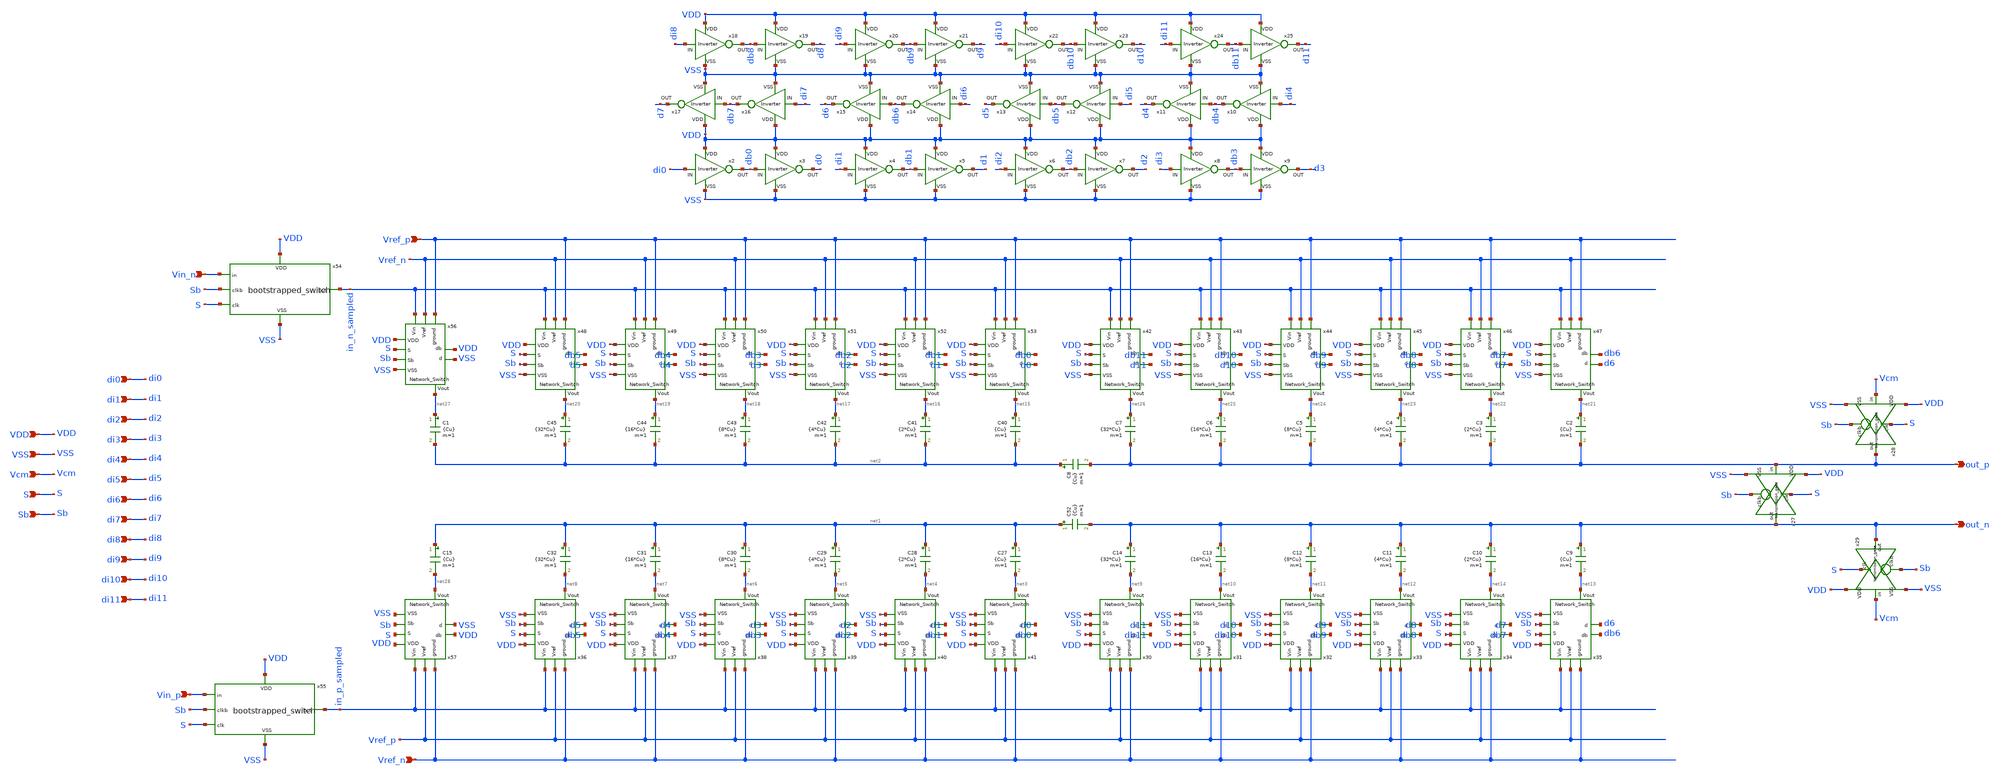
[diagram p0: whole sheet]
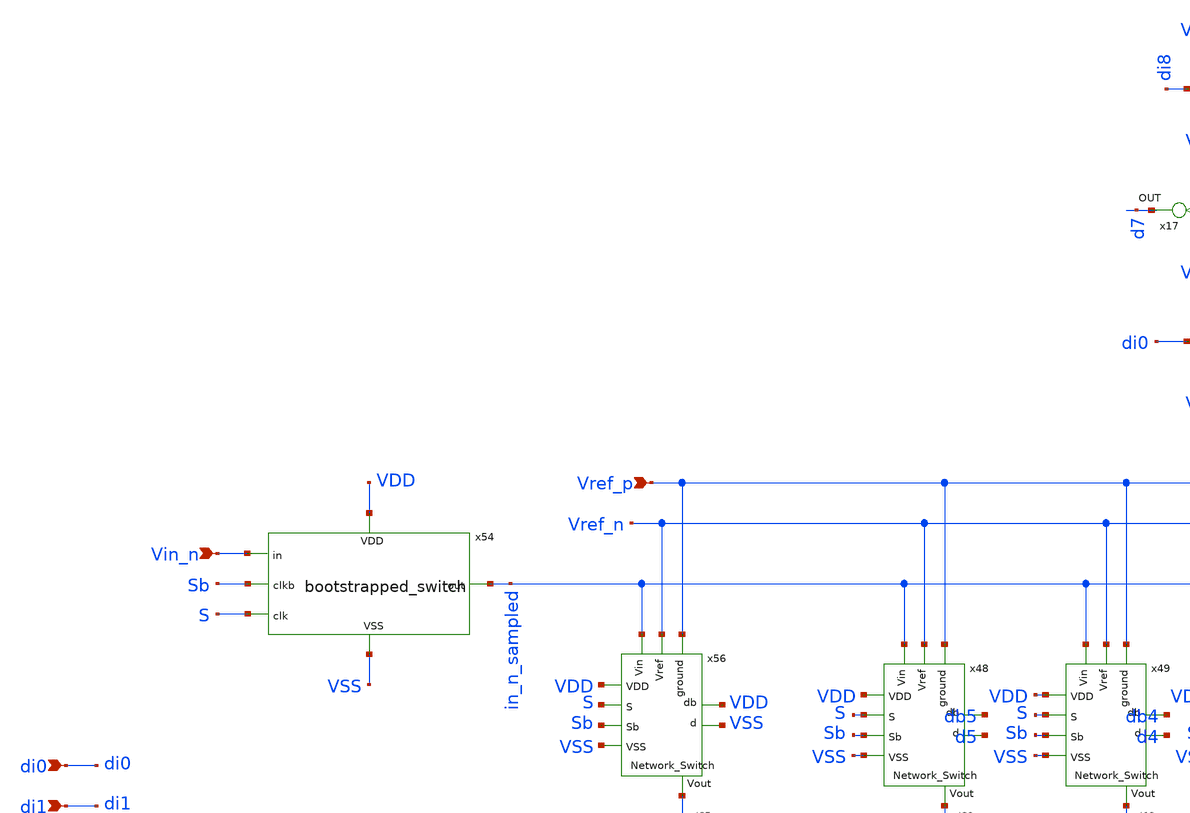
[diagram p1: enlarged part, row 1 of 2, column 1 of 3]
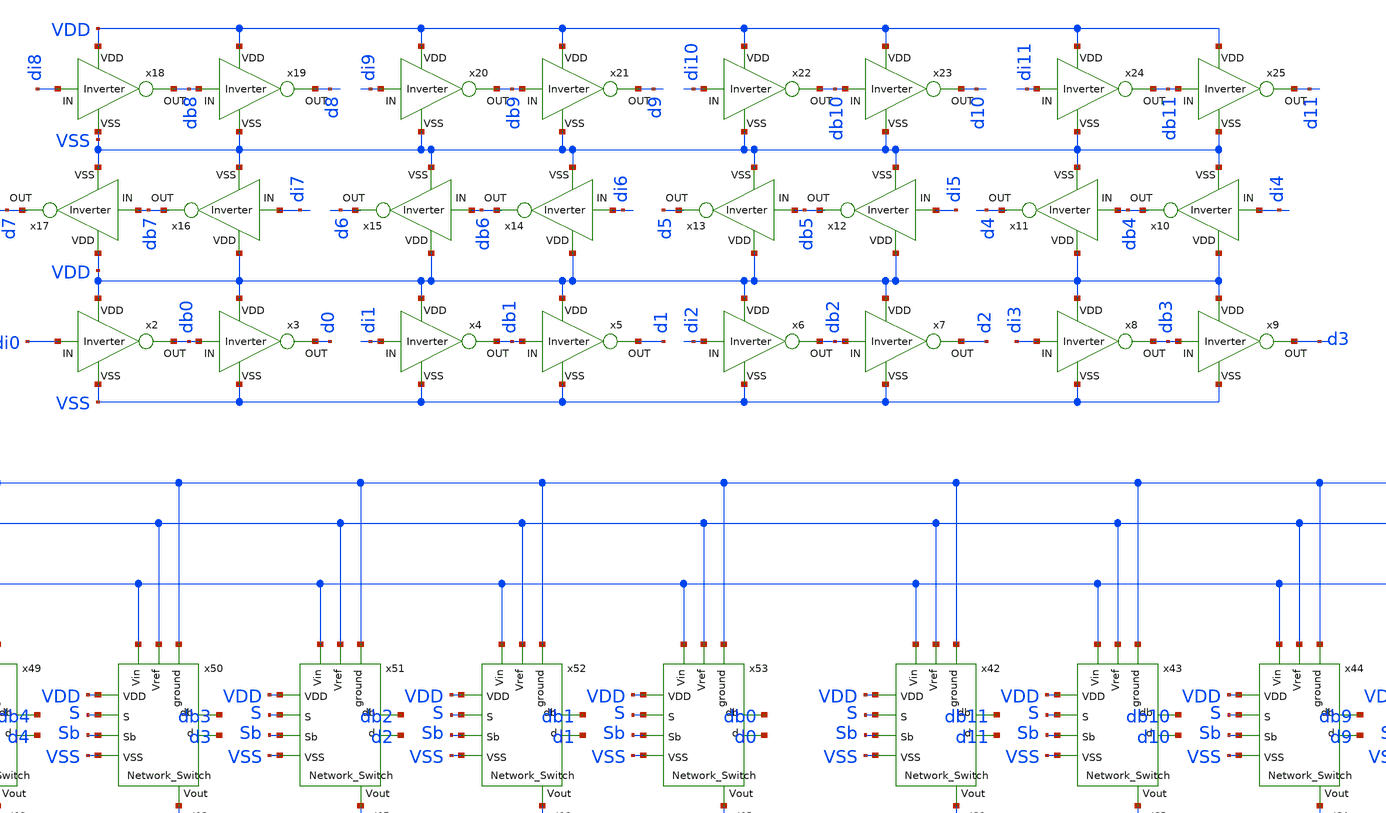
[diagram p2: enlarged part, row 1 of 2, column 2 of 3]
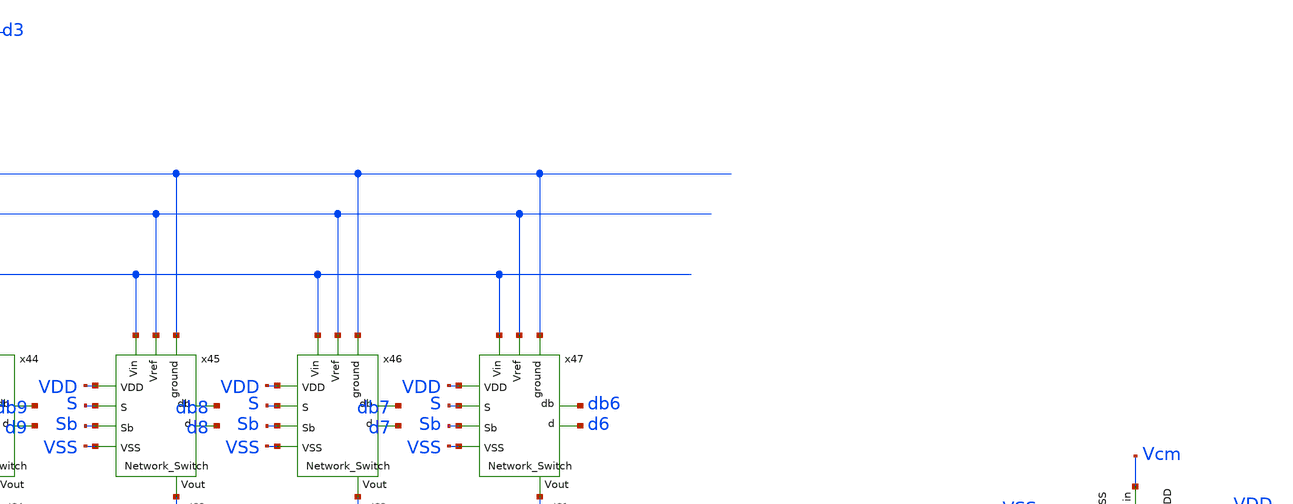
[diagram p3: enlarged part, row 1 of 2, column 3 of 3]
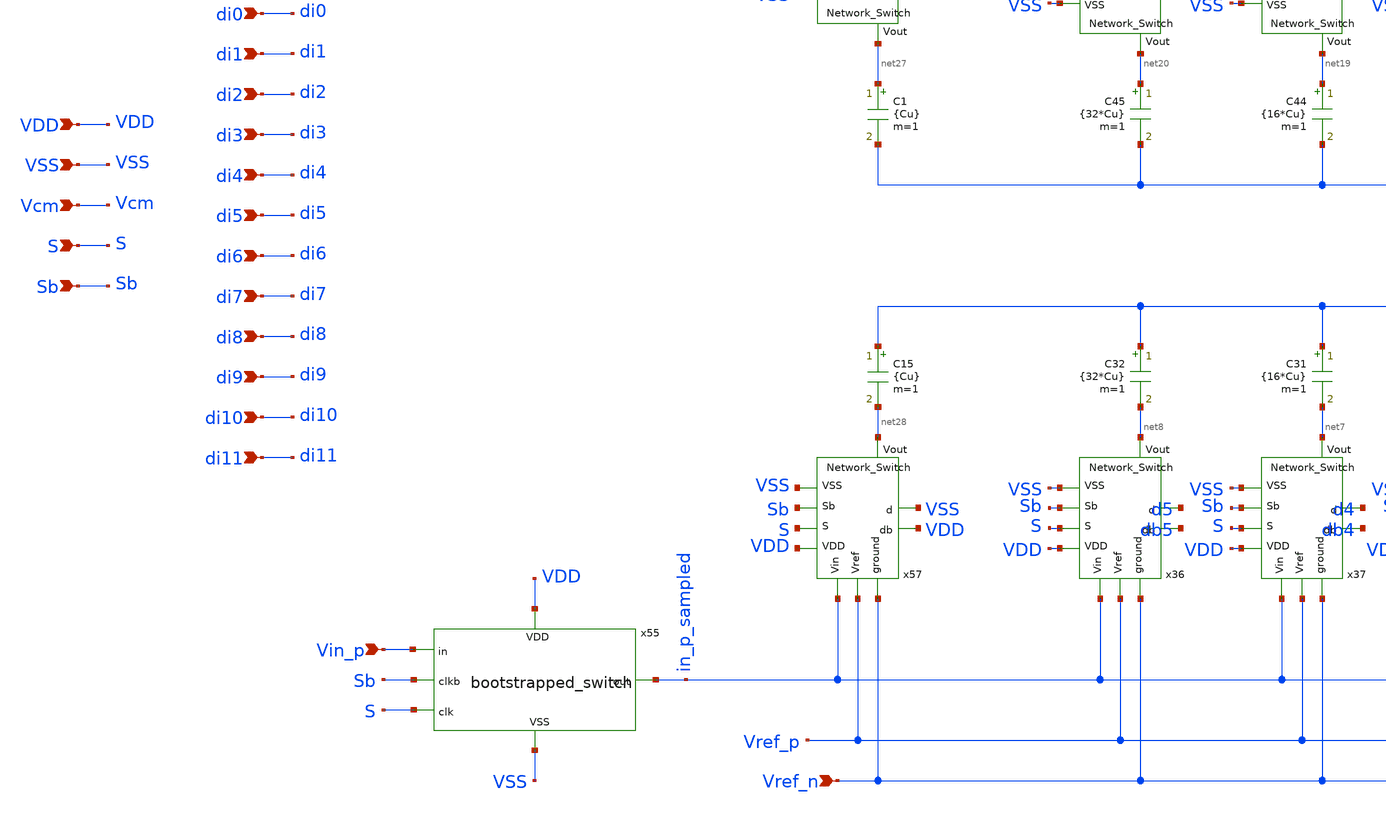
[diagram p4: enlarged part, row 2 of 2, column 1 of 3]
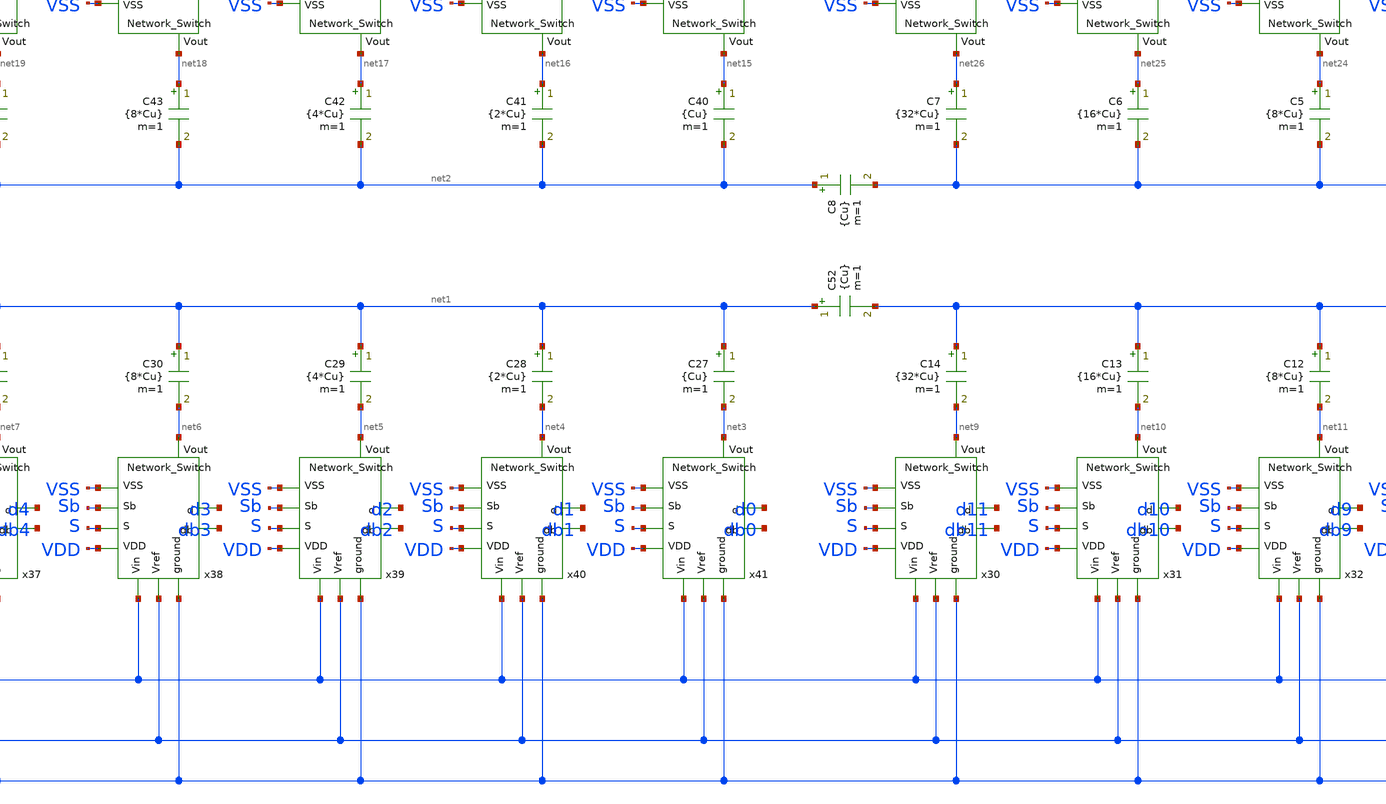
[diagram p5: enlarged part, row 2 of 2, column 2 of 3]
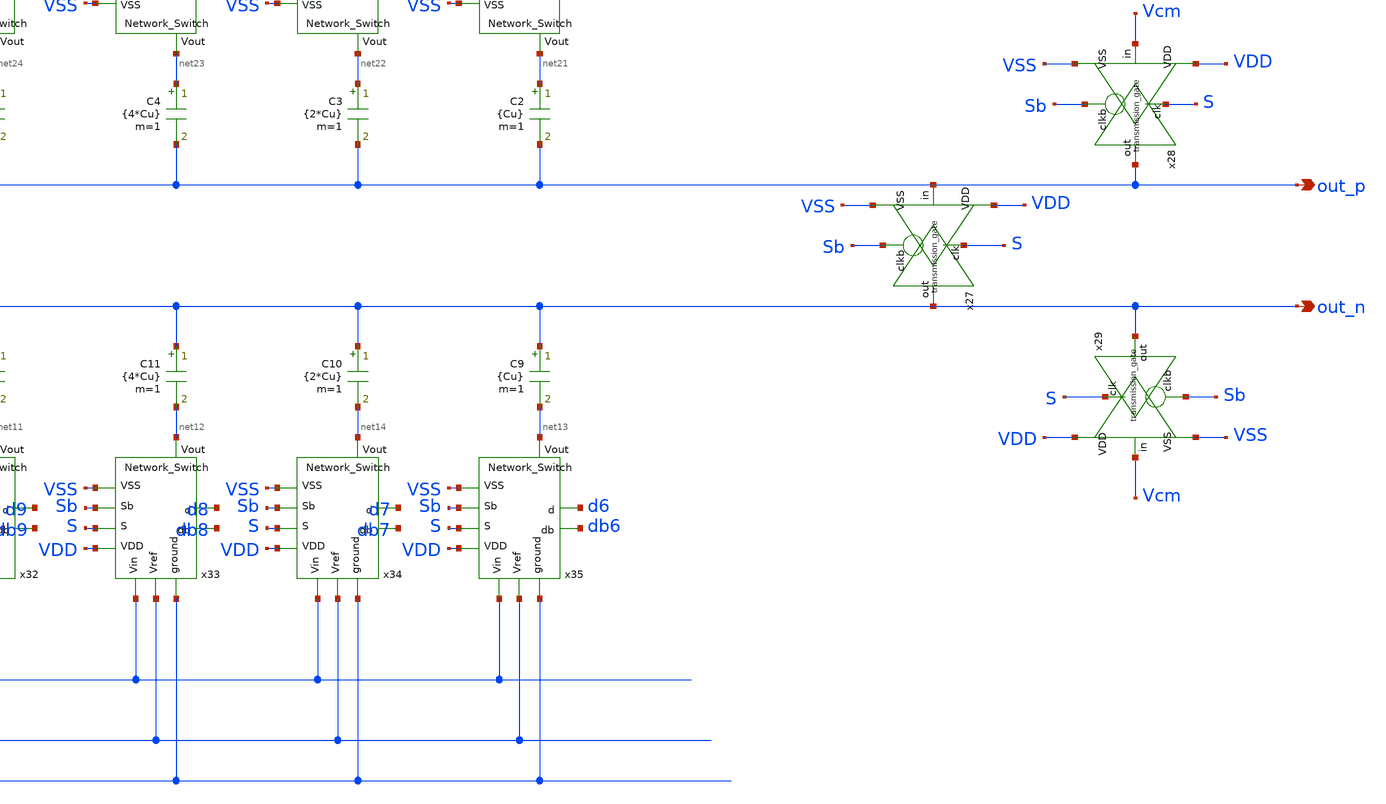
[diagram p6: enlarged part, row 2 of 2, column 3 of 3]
** sch_path: CAP_DAC_ideal_v2.sch
**.subckt CAP_DAC_ideal_v2 VDD VSS S Sb di3 Vcm out_p out_n Vref_p Vref_n di0 di1 di2 di5 di4 di7
*+ di6 di9 di8 di11 di10 Vin_n Vin_p
*.ipin VDD
*.ipin VSS
*.ipin S
*.ipin Sb
*.ipin di3
*.ipin Vcm
*.opin out_p
*.opin out_n
*.ipin Vref_p
*.ipin Vref_n
*.ipin di0
*.ipin di1
*.ipin di2
*.ipin di5
*.ipin di4
*.ipin di7
*.ipin di6
*.ipin di9
*.ipin di8
*.ipin di11
*.ipin di10
*.ipin Vin_n
*.ipin Vin_p
x30 VDD Vref_n Vref_p VSS S Sb d11 db11 in_p_sampled net9 Network_Switch
x31 VDD Vref_n Vref_p VSS S Sb d10 db10 in_p_sampled net10 Network_Switch
x32 VDD Vref_n Vref_p VSS S Sb d9 db9 in_p_sampled net11 Network_Switch
x33 VDD Vref_n Vref_p VSS S Sb d8 db8 in_p_sampled net12 Network_Switch
x34 VDD Vref_n Vref_p VSS S Sb d7 db7 in_p_sampled net14 Network_Switch
x35 VDD Vref_n Vref_p VSS S Sb d6 db6 in_p_sampled net13 Network_Switch
x36 VDD Vref_n Vref_p VSS S Sb d5 db5 in_p_sampled net8 Network_Switch
x37 VDD Vref_n Vref_p VSS S Sb d4 db4 in_p_sampled net7 Network_Switch
x38 VDD Vref_n Vref_p VSS S Sb d3 db3 in_p_sampled net6 Network_Switch
x39 VDD Vref_n Vref_p VSS S Sb d2 db2 in_p_sampled net5 Network_Switch
x40 VDD Vref_n Vref_p VSS S Sb d1 db1 in_p_sampled net4 Network_Switch
x41 VDD Vref_n Vref_p VSS S Sb d0 db0 in_p_sampled net3 Network_Switch
x42 VDD Vref_p Vref_n VSS S Sb d11 db11 in_n_sampled net26 Network_Switch
x43 VDD Vref_p Vref_n VSS S Sb d10 db10 in_n_sampled net25 Network_Switch
x44 VDD Vref_p Vref_n VSS S Sb d9 db9 in_n_sampled net24 Network_Switch
x45 VDD Vref_p Vref_n VSS S Sb d8 db8 in_n_sampled net23 Network_Switch
x46 VDD Vref_p Vref_n VSS S Sb d7 db7 in_n_sampled net22 Network_Switch
x47 VDD Vref_p Vref_n VSS S Sb d6 db6 in_n_sampled net21 Network_Switch
x48 VDD Vref_p Vref_n VSS S Sb d5 db5 in_n_sampled net20 Network_Switch
x49 VDD Vref_p Vref_n VSS S Sb d4 db4 in_n_sampled net19 Network_Switch
x50 VDD Vref_p Vref_n VSS S Sb d3 db3 in_n_sampled net18 Network_Switch
x51 VDD Vref_p Vref_n VSS S Sb d2 db2 in_n_sampled net17 Network_Switch
x52 VDD Vref_p Vref_n VSS S Sb d1 db1 in_n_sampled net16 Network_Switch
x53 VDD Vref_p Vref_n VSS S Sb d0 db0 in_n_sampled net15 Network_Switch
x54 VDD Vin_n Sb S in_n_sampled VSS bootstrapped_switch
x55 VDD Vin_p Sb S in_p_sampled VSS bootstrapped_switch
x27 out_p Sb S VDD VSS out_n transmission_gate
x2 VDD di0 db0 VSS Inverter
x3 VDD db0 d0 VSS Inverter
x4 VDD di1 db1 VSS Inverter
x5 VDD db1 d1 VSS Inverter
x6 VDD di2 db2 VSS Inverter
x7 VDD db2 d2 VSS Inverter
x8 VDD di3 db3 VSS Inverter
x9 VDD db3 d3 VSS Inverter
x10 VDD di4 db4 VSS Inverter
x11 VDD db4 d4 VSS Inverter
x12 VDD di5 db5 VSS Inverter
x13 VDD db5 d5 VSS Inverter
x14 VDD di6 db6 VSS Inverter
x15 VDD db6 d6 VSS Inverter
x16 VDD di7 db7 VSS Inverter
x17 VDD db7 d7 VSS Inverter
x18 VDD di8 db8 VSS Inverter
x19 VDD db8 d8 VSS Inverter
x20 VDD di9 db9 VSS Inverter
x21 VDD db9 d9 VSS Inverter
x22 VDD di10 db10 VSS Inverter
x23 VDD db10 d10 VSS Inverter
x24 VDD di11 db11 VSS Inverter
x25 VDD db11 d11 VSS Inverter
x28 Vcm Sb S VDD VSS out_p transmission_gate
x29 Vcm Sb S VDD VSS out_n transmission_gate
x56 VDD Vref_p Vref_n VSS S Sb VSS VDD in_n_sampled net27 Network_Switch
x57 VDD Vref_n Vref_p VSS S Sb VSS VDD in_p_sampled net28 Network_Switch
C40 net15 net2 {Cu} m=1
C41 net16 net2 {2*Cu} m=1
C42 net17 net2 {4*Cu} m=1
C43 net18 net2 {8*Cu} m=1
C44 net19 net2 {16*Cu} m=1
C45 net20 net2 {32*Cu} m=1
C52 net1 out_n {Cu} m=1
C27 net1 net3 {Cu} m=1
C28 net1 net4 {2*Cu} m=1
C29 net1 net5 {4*Cu} m=1
C30 net1 net6 {8*Cu} m=1
C31 net1 net7 {16*Cu} m=1
C32 net1 net8 {32*Cu} m=1
C2 net21 out_p {Cu} m=1
C3 net22 out_p {2*Cu} m=1
C4 net23 out_p {4*Cu} m=1
C5 net24 out_p {8*Cu} m=1
C6 net25 out_p {16*Cu} m=1
C7 net26 out_p {32*Cu} m=1
C8 net2 out_p {Cu} m=1
C9 out_n net13 {Cu} m=1
C10 out_n net14 {2*Cu} m=1
C11 out_n net12 {4*Cu} m=1
C12 out_n net11 {8*Cu} m=1
C13 out_n net10 {16*Cu} m=1
C14 out_n net9 {32*Cu} m=1
C1 net27 net2 {Cu} m=1
C15 net1 net28 {Cu} m=1
**.ends

* expanding   symbol:  Network_Switch.sym # of pins=10
** sym_path: Network_Switch.sym
** sch_path: Network_Switch.sch
.subckt Network_Switch VDD ground Vref VSS S Sb d db Vin Vout
*.ipin ground
*.ipin Vref
*.ipin Vin
*.opin Vout
*.ipin VDD
*.ipin VSS
*.ipin S
*.ipin Sb
*.ipin d
*.ipin db
x1 ground d db VDD VSS net1 transmission_gate
x2 Vref db d VDD VSS net1 transmission_gate
x3 net1 S Sb VDD VSS Vout transmission_gate
x4 Vin Sb S VDD VSS Vout transmission_gate
.ends


* expanding   symbol:  bootstrapped_switch.sym # of pins=6
** sym_path: bootstrapped_switch.sym
** sch_path: bootstrapped_switch.sch
.subckt bootstrapped_switch VDD in clkb clk out VSS
*.ipin in
*.opin out
*.ipin VSS
*.ipin VDD
*.ipin clkb
*.ipin clk
XM1 net4 clkb net5 net5 sky130_fd_pr__nfet_01v8 L=0.15 W=2 nf=1 ad='int((nf+1)/2) * W/nf * 0.29' as='int((nf+2)/2) * W/nf * 0.29'
+ pd='2*int((nf+1)/2) * (W/nf + 0.29)' ps='2*int((nf+2)/2) * (W/nf + 0.29)' nrd='0.29 / W' nrs='0.29 / W'
+ sa=0 sb=0 sd=0 mult=1 m=1
XM2 in Vg net4 VSS sky130_fd_pr__nfet_01v8 L=1 W=0.5 nf=1 ad='int((nf+1)/2) * W/nf * 0.29' as='int((nf+2)/2) * W/nf * 0.29'
+ pd='2*int((nf+1)/2) * (W/nf + 0.29)' ps='2*int((nf+2)/2) * (W/nf + 0.29)' nrd='0.29 / W' nrs='0.29 / W'
+ sa=0 sb=0 sd=0 mult=1 m=1
XM3 Vp Vg net1 Vp sky130_fd_pr__pfet_01v8 L=0.15 W=2 nf=1 ad='int((nf+1)/2) * W/nf * 0.29' as='int((nf+2)/2) * W/nf * 0.29'
+ pd='2*int((nf+1)/2) * (W/nf + 0.29)' ps='2*int((nf+2)/2) * (W/nf + 0.29)' nrd='0.29 / W' nrs='0.29 / W'
+ sa=0 sb=0 sd=0 mult=1 m=1
XM5 out Vg in VSS sky130_fd_pr__nfet_01v8 L=0.15 W=30 nf=1 ad='int((nf+1)/2) * W/nf * 0.29' as='int((nf+2)/2) * W/nf * 0.29'
+ pd='2*int((nf+1)/2) * (W/nf + 0.29)' ps='2*int((nf+2)/2) * (W/nf + 0.29)' nrd='0.29 / W' nrs='0.29 / W'
+ sa=0 sb=0 sd=0 mult=1 m=1
XM6 out clkb in VDD sky130_fd_pr__pfet_01v8 L=0.15 W=30 nf=1 ad='int((nf+1)/2) * W/nf * 0.29' as='int((nf+2)/2) * W/nf * 0.29'
+ pd='2*int((nf+1)/2) * (W/nf + 0.29)' ps='2*int((nf+2)/2) * (W/nf + 0.29)' nrd='0.29 / W' nrs='0.29 / W'
+ sa=0 sb=0 sd=0 mult=1 m=1
XM8 net6 clkb net2 net2 sky130_fd_pr__nfet_01v8 L=0.15 W=0.5 nf=1 ad='int((nf+1)/2) * W/nf * 0.29' as='int((nf+2)/2) * W/nf * 0.29'
+ pd='2*int((nf+1)/2) * (W/nf + 0.29)' ps='2*int((nf+2)/2) * (W/nf + 0.29)' nrd='0.29 / W' nrs='0.29 / W'
+ sa=0 sb=0 sd=0 mult=1 m=1
XC1 net4 Vp sky130_fd_pr__cap_mim_m3_1 W=18 L=18 MF=10 m=10
XM7 Vg VDD net6 net6 sky130_fd_pr__nfet_01v8 L=0.15 W=0.5 nf=1 ad='int((nf+1)/2) * W/nf * 0.29' as='int((nf+2)/2) * W/nf * 0.29'
+ pd='2*int((nf+1)/2) * (W/nf + 0.29)' ps='2*int((nf+2)/2) * (W/nf + 0.29)' nrd='0.29 / W' nrs='0.29 / W'
+ sa=0 sb=0 sd=0 mult=1 m=1
XM4 Vg net3 Vp Vp sky130_fd_pr__pfet_01v8 L=0.15 W=0.5 nf=1 ad='int((nf+1)/2) * W/nf * 0.29' as='int((nf+2)/2) * W/nf * 0.29'
+ pd='2*int((nf+1)/2) * (W/nf + 0.29)' ps='2*int((nf+2)/2) * (W/nf + 0.29)' nrd='0.29 / W' nrs='0.29 / W'
+ sa=0 sb=0 sd=0 mult=1 m=1
XC2 out VSS sky130_fd_pr__cap_mim_m3_1 W=36 L=36 MF=20 m=20
XM10 net1 clk net7 net1 sky130_fd_pr__pfet_01v8 L=0.15 W=2 nf=1 ad='int((nf+1)/2) * W/nf * 0.29' as='int((nf+2)/2) * W/nf * 0.29'
+ pd='2*int((nf+1)/2) * (W/nf + 0.29)' ps='2*int((nf+2)/2) * (W/nf + 0.29)' nrd='0.29 / W' nrs='0.29 / W'
+ sa=0 sb=0 sd=0 mult=1 m=1
XM11 net5 clkb net8 net8 sky130_fd_pr__nfet_01v8 L=0.15 W=2 nf=1 ad='int((nf+1)/2) * W/nf * 0.29' as='int((nf+2)/2) * W/nf * 0.29'
+ pd='2*int((nf+1)/2) * (W/nf + 0.29)' ps='2*int((nf+2)/2) * (W/nf + 0.29)' nrd='0.29 / W' nrs='0.29 / W'
+ sa=0 sb=0 sd=0 mult=1 m=1
XM12 net7 clk VDD net7 sky130_fd_pr__pfet_01v8 L=0.15 W=2 nf=1 ad='int((nf+1)/2) * W/nf * 0.29' as='int((nf+2)/2) * W/nf * 0.29'
+ pd='2*int((nf+1)/2) * (W/nf + 0.29)' ps='2*int((nf+2)/2) * (W/nf + 0.29)' nrd='0.29 / W' nrs='0.29 / W'
+ sa=0 sb=0 sd=0 mult=1 m=1
XM13 net8 clkb VSS VSS sky130_fd_pr__nfet_01v8 L=0.15 W=2 nf=1 ad='int((nf+1)/2) * W/nf * 0.29' as='int((nf+2)/2) * W/nf * 0.29'
+ pd='2*int((nf+1)/2) * (W/nf + 0.29)' ps='2*int((nf+2)/2) * (W/nf + 0.29)' nrd='0.29 / W' nrs='0.29 / W'
+ sa=0 sb=0 sd=0 mult=1 m=1
XM14 net2 clkb VSS VSS sky130_fd_pr__nfet_01v8 L=0.15 W=0.5 nf=1 ad='int((nf+1)/2) * W/nf * 0.29' as='int((nf+2)/2) * W/nf * 0.29'
+ pd='2*int((nf+1)/2) * (W/nf + 0.29)' ps='2*int((nf+2)/2) * (W/nf + 0.29)' nrd='0.29 / W' nrs='0.29 / W'
+ sa=0 sb=0 sd=0 mult=1 m=1
XM15 net3 clk VDD VDD sky130_fd_pr__pfet_01v8 L=0.15 W=1 nf=1 ad='int((nf+1)/2) * W/nf * 0.29' as='int((nf+2)/2) * W/nf * 0.29'
+ pd='2*int((nf+1)/2) * (W/nf + 0.29)' ps='2*int((nf+2)/2) * (W/nf + 0.29)' nrd='0.29 / W' nrs='0.29 / W'
+ sa=0 sb=0 sd=0 mult=1 m=1
XM16 net3 clk net4 VSS sky130_fd_pr__nfet_01v8 L=1 W=0.5 nf=1 ad='int((nf+1)/2) * W/nf * 0.29' as='int((nf+2)/2) * W/nf * 0.29'
+ pd='2*int((nf+1)/2) * (W/nf + 0.29)' ps='2*int((nf+2)/2) * (W/nf + 0.29)' nrd='0.29 / W' nrs='0.29 / W'
+ sa=0 sb=0 sd=0 mult=1 m=1
XM17 net3 Vg net4 VSS sky130_fd_pr__nfet_01v8 L=0.15 W=2 nf=1 ad='int((nf+1)/2) * W/nf * 0.29' as='int((nf+2)/2) * W/nf * 0.29'
+ pd='2*int((nf+1)/2) * (W/nf + 0.29)' ps='2*int((nf+2)/2) * (W/nf + 0.29)' nrd='0.29 / W' nrs='0.29 / W'
+ sa=0 sb=0 sd=0 mult=1 m=1
.ends


* expanding   symbol:  transmission_gate.sym # of pins=6
** sym_path: transmission_gate.sym
** sch_path: transmission_gate.sch
.subckt transmission_gate in clkb clk VDD VSS out
*.ipin in
*.ipin clk
*.ipin clkb
*.opin out
*.ipin VDD
*.ipin VSS
XM1 out clk in VSS sky130_fd_pr__nfet_01v8 L=0.15 W=0.5 nf=1 ad='int((nf+1)/2) * W/nf * 0.29' as='int((nf+2)/2) * W/nf * 0.29'
+ pd='2*int((nf+1)/2) * (W/nf + 0.29)' ps='2*int((nf+2)/2) * (W/nf + 0.29)' nrd='0.29 / W' nrs='0.29 / W'
+ sa=0 sb=0 sd=0 mult=1 m=1
XM2 out clkb in VDD sky130_fd_pr__pfet_01v8 L=0.15 W=0.5 nf=1 ad='int((nf+1)/2) * W/nf * 0.29' as='int((nf+2)/2) * W/nf * 0.29'
+ pd='2*int((nf+1)/2) * (W/nf + 0.29)' ps='2*int((nf+2)/2) * (W/nf + 0.29)' nrd='0.29 / W' nrs='0.29 / W'
+ sa=0 sb=0 sd=0 mult=1 m=1
.ends


* expanding   symbol:  Inverter.sym # of pins=4
** sym_path: Inverter.sym
** sch_path: Inverter.sch
.subckt Inverter VDD IN OUT VSS
*.ipin IN
*.ipin VSS
*.ipin VDD
*.opin OUT
XM1 OUT IN VSS VSS sky130_fd_pr__nfet_01v8 L=0.3 W=1 nf=1 ad='int((nf+1)/2) * W/nf * 0.29' as='int((nf+2)/2) * W/nf * 0.29'
+ pd='2*int((nf+1)/2) * (W/nf + 0.29)' ps='2*int((nf+2)/2) * (W/nf + 0.29)' nrd='0.29 / W' nrs='0.29 / W'
+ sa=0 sb=0 sd=0 mult=1 m=1
XM2 OUT IN VDD VDD sky130_fd_pr__pfet_01v8 L=0.3 W=2 nf=1 ad='int((nf+1)/2) * W/nf * 0.29' as='int((nf+2)/2) * W/nf * 0.29'
+ pd='2*int((nf+1)/2) * (W/nf + 0.29)' ps='2*int((nf+2)/2) * (W/nf + 0.29)' nrd='0.29 / W' nrs='0.29 / W'
+ sa=0 sb=0 sd=0 mult=1 m=1
.ends

.end
